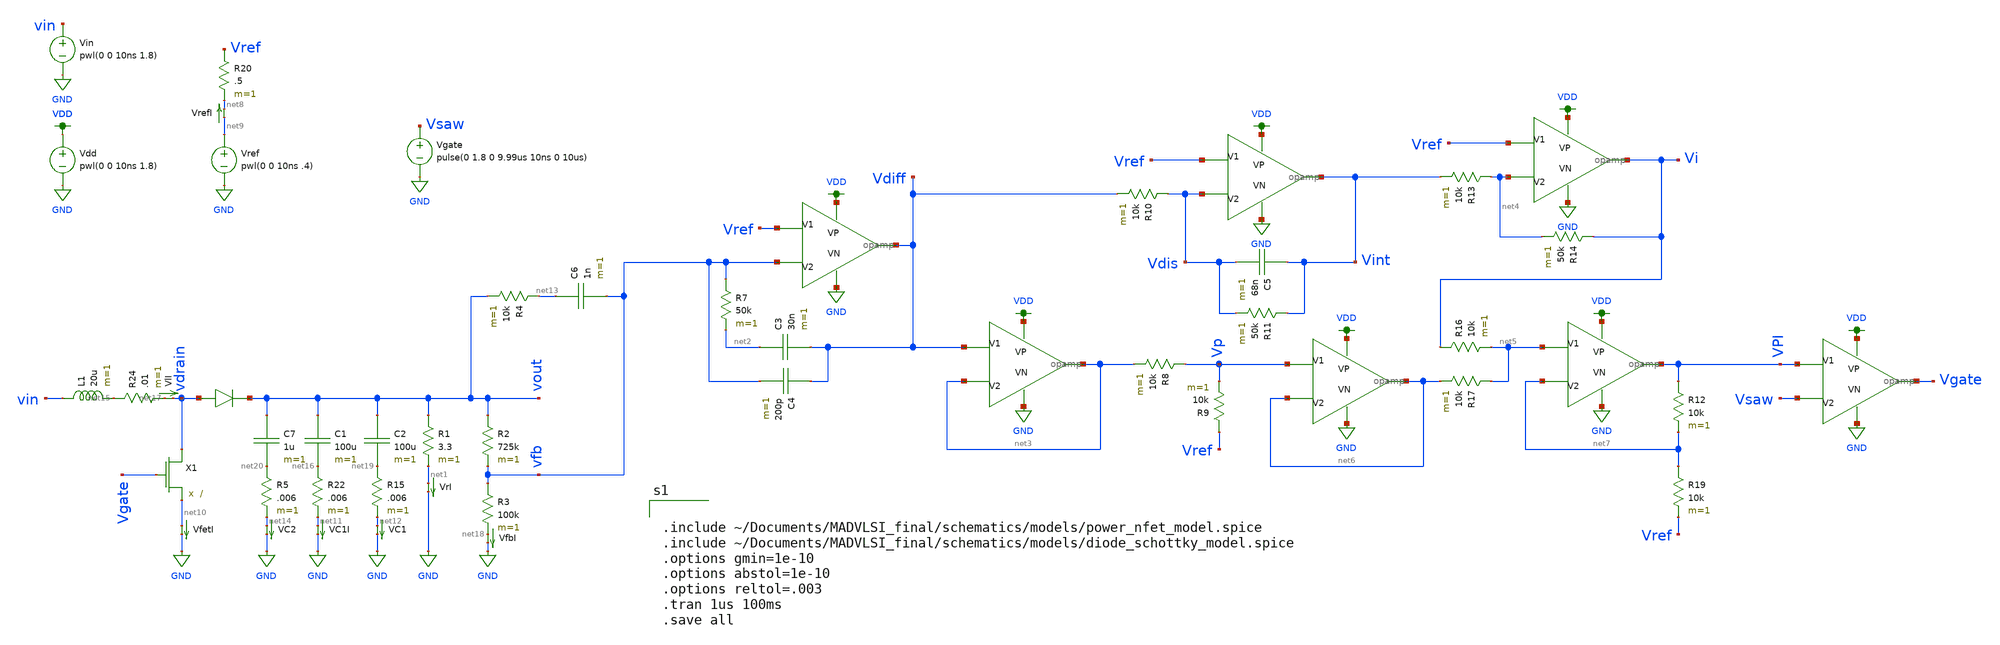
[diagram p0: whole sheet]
** sch_path: schematics/boost_VMC_tmp.sch
**.subckt boost_VMC_tmp
Vin vin GND pwl(0 0 10ns 1.8)
VfetI net10 GND 0
.save i(vfeti)
X1 vdrain Vgate net10 power_nfet
L1 vin net15 20u m=1
D1 vdrain vout diode_schottky
C1 vout net16 100u m=1
R1 vout net1 3.3 m=1
VlI net17 vdrain 0
.save i(vli)
VC1I net11 GND 0
.save i(vc1i)
VrI net1 GND 0
.save i(vri)
R2 vout vfb 725k m=1
R3 vfb net18 100k m=1
Vdd VDD GND pwl(0 0 10ns 1.8)
Vref net9 GND pwl(0 0 10ns .4)
R7 vfb net2 50k m=1
X3 Vref vfb VDD GND Vdiff opamp
X4 Vdiff net3 VDD GND net3 opamp
R8 Vp net3 10k m=1
R9 Vref Vp 10k m=1
X6 Vref Vdis VDD GND Vint opamp
R10 Vdis Vdiff 10k m=1
C5 Vint Vdis 68n m=1
R11 Vint Vdis 50k m=1
X7 Vref net4 VDD GND Vi opamp
R13 net4 Vint 10k m=1
R14 Vi net4 50k m=1
X8 net5 net7 VDD GND VPI opamp
R16 Vi net5 10k m=1
R17 net5 net6 10k m=1
X9 Vp net6 VDD GND net6 opamp
R19 net7 Vref 10k m=1
X11 VPI Vsaw VDD GND Vgate opamp
Vgate Vsaw GND pulse(0 1.8 0 9.99us 10ns 0 10us)
VrefI net9 net8 0
.save i(vrefi)
R22 net16 net11 .006 m=1
R24 net15 net17 .01 m=1
VfbI net18 GND 0
.save i(vfbi)
R20 Vref net8 .5 m=1
R12 VPI net7 10k m=1
C2 vout net19 100u m=1
VC1 net12 GND 0
.save i(vc1)
R15 net19 net12 .006 m=1
C3 net2 Vdiff 30n m=1
C4 Vdiff vfb 200p m=1
R4 net13 vout 10k m=1
C6 net13 vfb 1n m=1
C7 vout net20 1u m=1
R5 net20 net14 .006 m=1
VC2 net14 GND 0
.save i(vc2)
**** begin user architecture code


.include ~/Documents/MADVLSI_final/schematics/models/power_nfet_model.spice
.include ~/Documents/MADVLSI_final/schematics/models/diode_schottky_model.spice
.options gmin=1e-10
.options abstol=1e-10
.options reltol=.003
.tran 1us 100ms
.save all


.option wnflag=1
.lib ~/skywater/skywater-pdk/libraries/sky130_fd_pr_ngspice/latest/models/sky130.lib.spice tt

**** end user architecture code
**.ends

* expanding   symbol:  /home/madvlsi/Documents/MADVLSI_final/schematics/opamp.sym # of pins=5
** sym_path: schematics/opamp.sym
** sch_path: schematics/opamp.sch
.subckt opamp V1 V2 VP VN Vout
*.ipin V1
*.ipin V2
*.opin Vout
*.iopin VP
*.iopin VN
*.iopin VP
*.iopin VN
XM1 VN net7 net2 GND sky130_fd_pr__nfet_01v8 L=l W=w nf=1 ad='int((nf+1)/2) * W/nf * 0.29' as='int((nf+2)/2) * W/nf * 0.29'
+ pd='2*int((nf+1)/2) * (W/nf + 0.29)' ps='2*int((nf+2)/2) * (W/nf + 0.29)' nrd='0.29 / W' nrs='0.29 / W'
+ sa=0 sb=0 sd=0 mult=1 m=1
XM2 VP net3 net1 VDD sky130_fd_pr__pfet_01v8 L=l W=w nf=1 ad='int((nf+1)/2) * W/nf * 0.29' as='int((nf+2)/2) * W/nf * 0.29'
+ pd='2*int((nf+1)/2) * (W/nf + 0.29)' ps='2*int((nf+2)/2) * (W/nf + 0.29)' nrd='0.29 / W' nrs='0.29 / W'
+ sa=0 sb=0 sd=0 mult=1 m=1
XM3 net1 V1 Vd VDD sky130_fd_pr__pfet_01v8 L=l W=w nf=1 ad='int((nf+1)/2) * W/nf * 0.29' as='int((nf+2)/2) * W/nf * 0.29'
+ pd='2*int((nf+1)/2) * (W/nf + 0.29)' ps='2*int((nf+2)/2) * (W/nf + 0.29)' nrd='0.29 / W' nrs='0.29 / W'
+ sa=0 sb=0 sd=0 mult=1 m=1
XM4 Vc V2 net1 VDD sky130_fd_pr__pfet_01v8 L=l W=w nf=1 ad='int((nf+1)/2) * W/nf * 0.29' as='int((nf+2)/2) * W/nf * 0.29'
+ pd='2*int((nf+1)/2) * (W/nf + 0.29)' ps='2*int((nf+2)/2) * (W/nf + 0.29)' nrd='0.29 / W' nrs='0.29 / W'
+ sa=0 sb=0 sd=0 mult=1 m=1
XM5 Va V2 net2 GND sky130_fd_pr__nfet_01v8 L=l W=w nf=1 ad='int((nf+1)/2) * W/nf * 0.29' as='int((nf+2)/2) * W/nf * 0.29'
+ pd='2*int((nf+1)/2) * (W/nf + 0.29)' ps='2*int((nf+2)/2) * (W/nf + 0.29)' nrd='0.29 / W' nrs='0.29 / W'
+ sa=0 sb=0 sd=0 mult=1 m=1
XM6 net2 V1 Vb GND sky130_fd_pr__nfet_01v8 L=l W=w nf=1 ad='int((nf+1)/2) * W/nf * 0.29' as='int((nf+2)/2) * W/nf * 0.29'
+ pd='2*int((nf+1)/2) * (W/nf + 0.29)' ps='2*int((nf+2)/2) * (W/nf + 0.29)' nrd='0.29 / W' nrs='0.29 / W'
+ sa=0 sb=0 sd=0 mult=1 m=1
XM7 net3 net3 Va VDD sky130_fd_pr__pfet_01v8 L=l W=w nf=1 ad='int((nf+1)/2) * W/nf * 0.29' as='int((nf+2)/2) * W/nf * 0.29'
+ pd='2*int((nf+1)/2) * (W/nf + 0.29)' ps='2*int((nf+2)/2) * (W/nf + 0.29)' nrd='0.29 / W' nrs='0.29 / W'
+ sa=0 sb=0 sd=0 mult=1 m=1
XM8 net6 net6 Va VDD sky130_fd_pr__pfet_01v8 L=l W=w nf=1 ad='int((nf+1)/2) * W/nf * 0.29' as='int((nf+2)/2) * W/nf * 0.29'
+ pd='2*int((nf+1)/2) * (W/nf + 0.29)' ps='2*int((nf+2)/2) * (W/nf + 0.29)' nrd='0.29 / W' nrs='0.29 / W'
+ sa=0 sb=0 sd=0 mult=1 m=1
XM9 net5 net6 Vb VDD sky130_fd_pr__pfet_01v8 L=l W=w nf=1 ad='int((nf+1)/2) * W/nf * 0.29' as='int((nf+2)/2) * W/nf * 0.29'
+ pd='2*int((nf+1)/2) * (W/nf + 0.29)' ps='2*int((nf+2)/2) * (W/nf + 0.29)' nrd='0.29 / W' nrs='0.29 / W'
+ sa=0 sb=0 sd=0 mult=1 m=1
XM10 Va net3 VP VDD sky130_fd_pr__pfet_01v8 L=l W=w nf=1 ad='int((nf+1)/2) * W/nf * 0.29' as='int((nf+2)/2) * W/nf * 0.29'
+ pd='2*int((nf+1)/2) * (W/nf + 0.29)' ps='2*int((nf+2)/2) * (W/nf + 0.29)' nrd='0.29 / W' nrs='0.29 / W'
+ sa=0 sb=0 sd=0 mult=1 m=1
XM11 Vb net3 VP VDD sky130_fd_pr__pfet_01v8 L=l W=w nf=1 ad='int((nf+1)/2) * W/nf * 0.29' as='int((nf+2)/2) * W/nf * 0.29'
+ pd='2*int((nf+1)/2) * (W/nf + 0.29)' ps='2*int((nf+2)/2) * (W/nf + 0.29)' nrd='0.29 / W' nrs='0.29 / W'
+ sa=0 sb=0 sd=0 mult=1 m=1
XM12 net6 net6 Vc GND sky130_fd_pr__nfet_01v8 L=l W=w nf=1 ad='int((nf+1)/2) * W/nf * 0.29' as='int((nf+2)/2) * W/nf * 0.29'
+ pd='2*int((nf+1)/2) * (W/nf + 0.29)' ps='2*int((nf+2)/2) * (W/nf + 0.29)' nrd='0.29 / W' nrs='0.29 / W'
+ sa=0 sb=0 sd=0 mult=1 m=1
XM13 net5 net6 Vd GND sky130_fd_pr__nfet_01v8 L=l W=w nf=1 ad='int((nf+1)/2) * W/nf * 0.29' as='int((nf+2)/2) * W/nf * 0.29'
+ pd='2*int((nf+1)/2) * (W/nf + 0.29)' ps='2*int((nf+2)/2) * (W/nf + 0.29)' nrd='0.29 / W' nrs='0.29 / W'
+ sa=0 sb=0 sd=0 mult=1 m=1
XM14 Vc net7 VN GND sky130_fd_pr__nfet_01v8 L=l W=w nf=1 ad='int((nf+1)/2) * W/nf * 0.29' as='int((nf+2)/2) * W/nf * 0.29'
+ pd='2*int((nf+1)/2) * (W/nf + 0.29)' ps='2*int((nf+2)/2) * (W/nf + 0.29)' nrd='0.29 / W' nrs='0.29 / W'
+ sa=0 sb=0 sd=0 mult=1 m=1
XM15 Vd net7 VN GND sky130_fd_pr__nfet_01v8 L=l W=w nf=1 ad='int((nf+1)/2) * W/nf * 0.29' as='int((nf+2)/2) * W/nf * 0.29'
+ pd='2*int((nf+1)/2) * (W/nf + 0.29)' ps='2*int((nf+2)/2) * (W/nf + 0.29)' nrd='0.29 / W' nrs='0.29 / W'
+ sa=0 sb=0 sd=0 mult=1 m=1
XM16 net8 net7 net3 GND sky130_fd_pr__nfet_01v8 L=l W=w nf=1 ad='int((nf+1)/2) * W/nf * 0.29' as='int((nf+2)/2) * W/nf * 0.29'
+ pd='2*int((nf+1)/2) * (W/nf + 0.29)' ps='2*int((nf+2)/2) * (W/nf + 0.29)' nrd='0.29 / W' nrs='0.29 / W'
+ sa=0 sb=0 sd=0 mult=1 m=1
XM17 VN net7 net8 GND sky130_fd_pr__nfet_01v8 L=l W=w nf=1 ad='int((nf+1)/2) * W/nf * 0.29' as='int((nf+2)/2) * W/nf * 0.29'
+ pd='2*int((nf+1)/2) * (W/nf + 0.29)' ps='2*int((nf+2)/2) * (W/nf + 0.29)' nrd='0.29 / W' nrs='0.29 / W'
+ sa=0 sb=0 sd=0 mult=1 m=1
XM18 net8 net7 VP GND sky130_fd_pr__nfet_01v8 L=l W=w nf=1 ad='int((nf+1)/2) * W/nf * 0.29' as='int((nf+2)/2) * W/nf * 0.29'
+ pd='2*int((nf+1)/2) * (W/nf + 0.29)' ps='2*int((nf+2)/2) * (W/nf + 0.29)' nrd='0.29 / W' nrs='0.29 / W'
+ sa=0 sb=0 sd=0 mult=M m=M
XM19 net4 net3 net7 VDD sky130_fd_pr__pfet_01v8 L=l W=w nf=1 ad='int((nf+1)/2) * W/nf * 0.29' as='int((nf+2)/2) * W/nf * 0.29'
+ pd='2*int((nf+1)/2) * (W/nf + 0.29)' ps='2*int((nf+2)/2) * (W/nf + 0.29)' nrd='0.29 / W' nrs='0.29 / W'
+ sa=0 sb=0 sd=0 mult=1 m=1
XM20 VP net3 net4 VDD sky130_fd_pr__pfet_01v8 L=l W=w nf=1 ad='int((nf+1)/2) * W/nf * 0.29' as='int((nf+2)/2) * W/nf * 0.29'
+ pd='2*int((nf+1)/2) * (W/nf + 0.29)' ps='2*int((nf+2)/2) * (W/nf + 0.29)' nrd='0.29 / W' nrs='0.29 / W'
+ sa=0 sb=0 sd=0 mult=1 m=1
XM21 net4 net3 VN VDD sky130_fd_pr__pfet_01v8 L=l W=w nf=1 ad='int((nf+1)/2) * W/nf * 0.29' as='int((nf+2)/2) * W/nf * 0.29'
+ pd='2*int((nf+1)/2) * (W/nf + 0.29)' ps='2*int((nf+2)/2) * (W/nf + 0.29)' nrd='0.29 / W' nrs='0.29 / W'
+ sa=0 sb=0 sd=0 mult=M m=M
XM22 net7 net7 Vc GND sky130_fd_pr__nfet_01v8 L=l W=w nf=1 ad='int((nf+1)/2) * W/nf * 0.29' as='int((nf+2)/2) * W/nf * 0.29'
+ pd='2*int((nf+1)/2) * (W/nf + 0.29)' ps='2*int((nf+2)/2) * (W/nf + 0.29)' nrd='0.29 / W' nrs='0.29 / W'
+ sa=0 sb=0 sd=0 mult=1 m=1
**** begin user architecture code

.param M=3
.param w=3
.param l=0.6


**** end user architecture code
XM23 Vout net5 VN GND sky130_fd_pr__nfet_01v8 L=.15 W=6 nf=1 ad='int((nf+1)/2) * W/nf * 0.29' as='int((nf+2)/2) * W/nf * 0.29'
+ pd='2*int((nf+1)/2) * (W/nf + 0.29)' ps='2*int((nf+2)/2) * (W/nf + 0.29)' nrd='0.29 / W' nrs='0.29 / W'
+ sa=0 sb=0 sd=0 mult=1 m=1
XM24 Vout net5 VP VDD sky130_fd_pr__pfet_01v8 L=.15 W=12 nf=1 ad='int((nf+1)/2) * W/nf * 0.29' as='int((nf+2)/2) * W/nf * 0.29'
+ pd='2*int((nf+1)/2) * (W/nf + 0.29)' ps='2*int((nf+2)/2) * (W/nf + 0.29)' nrd='0.29 / W' nrs='0.29 / W'
+ sa=0 sb=0 sd=0 mult=1 m=1
C1 Vout net5 500f m=1
.ends

.GLOBAL GND
.GLOBAL VDD
.end
